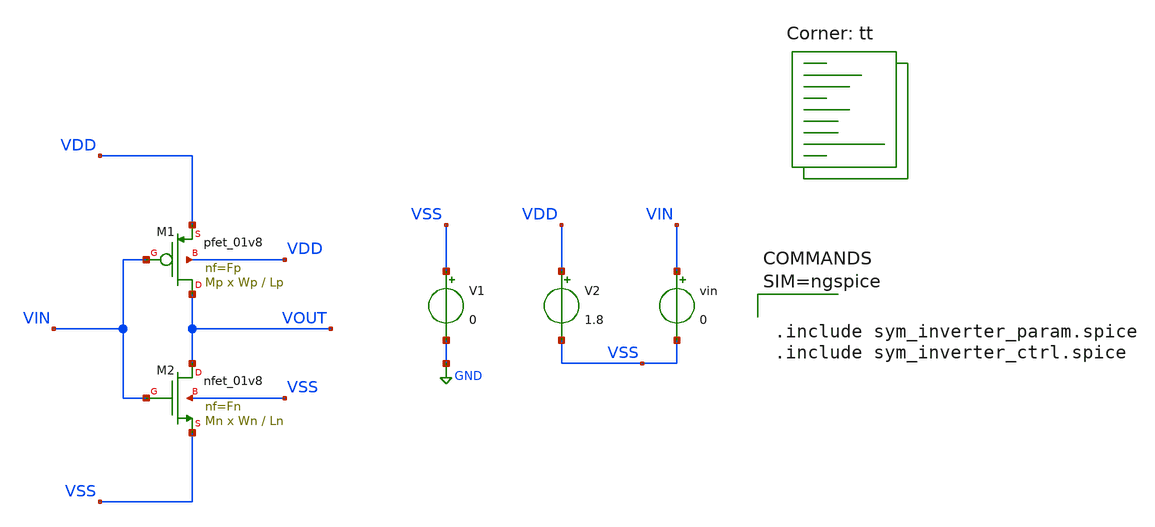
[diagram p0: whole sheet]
** sch_path: work/design/sym_inverter.sch
**.subckt sym_inverter
V1 VSS GND 0
V2 VDD VSS 1.8
vin VIN VSS 0
XM1 VOUT VIN VDD VDD sky130_fd_pr__pfet_01v8 L=Lp W=Wp nf=Fp ad='int((nf+1)/2) * W/nf * 0.29' as='int((nf+2)/2) * W/nf * 0.29'
+ pd='2*int((nf+1)/2) * (W/nf + 0.29)' ps='2*int((nf+2)/2) * (W/nf + 0.29)' nrd='0.29 / W' nrs='0.29 / W'
+ sa=0 sb=0 sd=0 mult=Mp m=Mp
XM2 VOUT VIN VSS VSS sky130_fd_pr__nfet_01v8 L=Ln W=Wn nf=Fn ad='int((nf+1)/2) * W/nf * 0.29' as='int((nf+2)/2) * W/nf * 0.29'
+ pd='2*int((nf+1)/2) * (W/nf + 0.29)' ps='2*int((nf+2)/2) * (W/nf + 0.29)' nrd='0.29 / W' nrs='0.29 / W'
+ sa=0 sb=0 sd=0 mult=Mn m=Mn
**** begin user architecture code
.lib $::SKYWATER_MODELS/sky130.lib.spice tt



.include sym_inverter_param.spice
.include sym_inverter_ctrl.spice



**** end user architecture code
**.ends
.GLOBAL GND
.end
